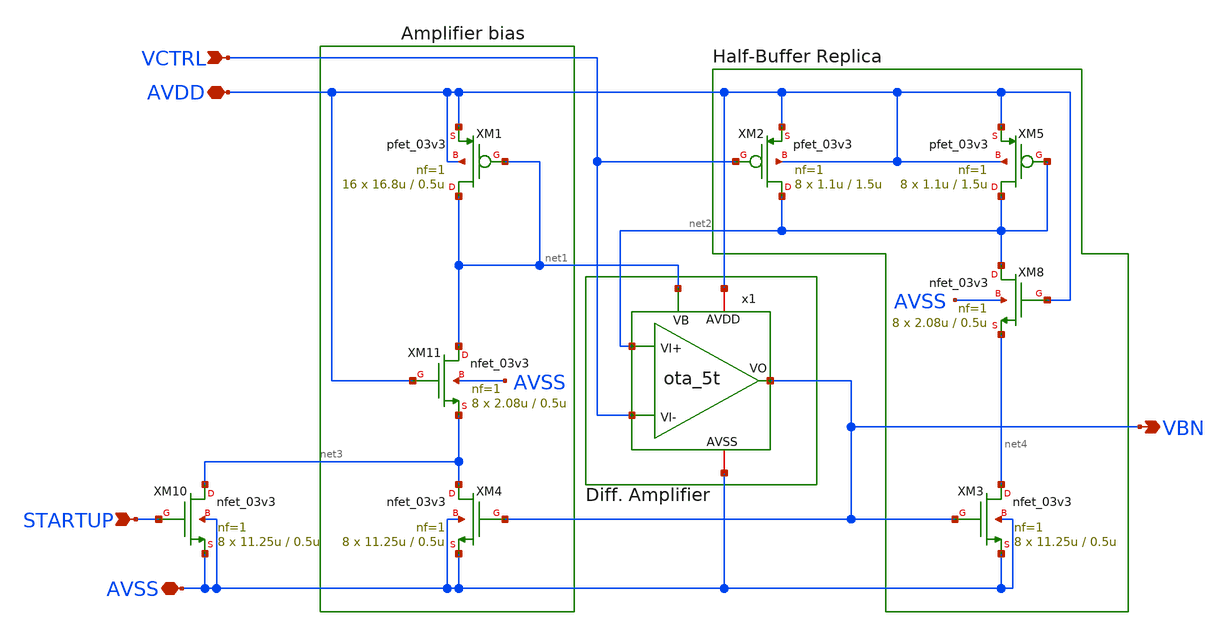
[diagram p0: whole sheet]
** sch_path: designs/libs/core_analog/bias_generator/bias_generator.sch
**.subckt bias_generator VCTRL STARTUP AVDD AVSS VBN
*.ipin VCTRL
*.ipin STARTUP
*.iopin AVDD
*.iopin AVSS
*.opin VBN
x1 VBN AVDD net2 VCTRL AVSS net1 ota_5t
XM1 net1 net1 AVDD AVDD pfet_03v3 L=0.5u W=16.8u nf=1 ad='int((nf+1)/2) * W/nf * 0.18u' as='int((nf+2)/2) * W/nf * 0.18u'
+ pd='2*int((nf+1)/2) * (W/nf + 0.18u)' ps='2*int((nf+2)/2) * (W/nf + 0.18u)' nrd='0.18u / W' nrs='0.18u / W'
+ sa=0 sb=0 sd=0 m=16
XM8 net2 AVDD net4 AVSS nfet_03v3 L=0.5u W=2.08u nf=1 ad='int((nf+1)/2) * W/nf * 0.18u' as='int((nf+2)/2) * W/nf * 0.18u'
+ pd='2*int((nf+1)/2) * (W/nf + 0.18u)' ps='2*int((nf+2)/2) * (W/nf + 0.18u)' nrd='0.18u / W' nrs='0.18u / W'
+ sa=0 sb=0 sd=0 m=8
XM11 net1 AVDD net3 AVSS nfet_03v3 L=0.5u W=2.08u nf=1 ad='int((nf+1)/2) * W/nf * 0.18u' as='int((nf+2)/2) * W/nf * 0.18u'
+ pd='2*int((nf+1)/2) * (W/nf + 0.18u)' ps='2*int((nf+2)/2) * (W/nf + 0.18u)' nrd='0.18u / W' nrs='0.18u / W'
+ sa=0 sb=0 sd=0 m=8
XM3 net4 VBN AVSS AVSS nfet_03v3 L=0.5u W=11.25u nf=1 ad='int((nf+1)/2) * W/nf * 0.18u' as='int((nf+2)/2) * W/nf * 0.18u'
+ pd='2*int((nf+1)/2) * (W/nf + 0.18u)' ps='2*int((nf+2)/2) * (W/nf + 0.18u)' nrd='0.18u / W' nrs='0.18u / W'
+ sa=0 sb=0 sd=0 m=8
XM4 net3 VBN AVSS AVSS nfet_03v3 L=0.5u W=11.25u nf=1 ad='int((nf+1)/2) * W/nf * 0.18u' as='int((nf+2)/2) * W/nf * 0.18u'
+ pd='2*int((nf+1)/2) * (W/nf + 0.18u)' ps='2*int((nf+2)/2) * (W/nf + 0.18u)' nrd='0.18u / W' nrs='0.18u / W'
+ sa=0 sb=0 sd=0 m=8
XM10 net3 STARTUP AVSS AVSS nfet_03v3 L=0.5u W=11.25u nf=1 ad='int((nf+1)/2) * W/nf * 0.18u' as='int((nf+2)/2) * W/nf * 0.18u'
+ pd='2*int((nf+1)/2) * (W/nf + 0.18u)' ps='2*int((nf+2)/2) * (W/nf + 0.18u)' nrd='0.18u / W' nrs='0.18u / W'
+ sa=0 sb=0 sd=0 m=8
XM2 net2 VCTRL AVDD AVDD pfet_03v3 L=1.5u W=1.1u nf=1 ad='int((nf+1)/2) * W/nf * 0.18u' as='int((nf+2)/2) * W/nf * 0.18u'
+ pd='2*int((nf+1)/2) * (W/nf + 0.18u)' ps='2*int((nf+2)/2) * (W/nf + 0.18u)' nrd='0.18u / W' nrs='0.18u / W'
+ sa=0 sb=0 sd=0 m=8
XM5 net2 net2 AVDD AVDD pfet_03v3 L=1.5u W=1.1u nf=1 ad='int((nf+1)/2) * W/nf * 0.18u' as='int((nf+2)/2) * W/nf * 0.18u'
+ pd='2*int((nf+1)/2) * (W/nf + 0.18u)' ps='2*int((nf+2)/2) * (W/nf + 0.18u)' nrd='0.18u / W' nrs='0.18u / W'
+ sa=0 sb=0 sd=0 m=8
**.ends

* expanding   symbol:  libs/core_analog/ota_5t/ota_5t.sym # of pins=6
** sym_path: designs/libs/core_analog/ota_5t/ota_5t.sym
** sch_path: designs/libs/core_analog/ota_5t/ota_5t.sch
.subckt ota_5t VO AVDD VI+ VI- AVSS VB
*.ipin VI+
*.ipin VI-
*.ipin VB
*.iopin AVDD
*.iopin AVSS
*.opin VO
XM1 VO VI- net2 AVDD pfet_03v3 L=0.5u W=6.55u nf=1 ad='int((nf+1)/2) * W/nf * 0.18u' as='int((nf+2)/2) * W/nf * 0.18u'
+ pd='2*int((nf+1)/2) * (W/nf + 0.18u)' ps='2*int((nf+2)/2) * (W/nf + 0.18u)' nrd='0.18u / W' nrs='0.18u / W'
+ sa=0 sb=0 sd=0 m=8
XM4 VO net1 AVSS AVSS nfet_03v3 L=0.5u W=4.8u nf=1 ad='int((nf+1)/2) * W/nf * 0.18u' as='int((nf+2)/2) * W/nf * 0.18u'
+ pd='2*int((nf+1)/2) * (W/nf + 0.18u)' ps='2*int((nf+2)/2) * (W/nf + 0.18u)' nrd='0.18u / W' nrs='0.18u / W'
+ sa=0 sb=0 sd=0 m=4
XM3 net2 VB net3 AVDD pfet_03v3 L=0.5u W=8.3u nf=1 ad='int((nf+1)/2) * W/nf * 0.18u' as='int((nf+2)/2) * W/nf * 0.18u'
+ pd='2*int((nf+1)/2) * (W/nf + 0.18u)' ps='2*int((nf+2)/2) * (W/nf + 0.18u)' nrd='0.18u / W' nrs='0.18u / W'
+ sa=0 sb=0 sd=0 m=16
XM2 net1 VI+ net2 AVDD pfet_03v3 L=0.5u W=6.55u nf=1 ad='int((nf+1)/2) * W/nf * 0.18u' as='int((nf+2)/2) * W/nf * 0.18u'
+ pd='2*int((nf+1)/2) * (W/nf + 0.18u)' ps='2*int((nf+2)/2) * (W/nf + 0.18u)' nrd='0.18u / W' nrs='0.18u / W'
+ sa=0 sb=0 sd=0 m=8
XM5 net1 net1 AVSS AVSS nfet_03v3 L=0.5u W=4.8u nf=1 ad='int((nf+1)/2) * W/nf * 0.18u' as='int((nf+2)/2) * W/nf * 0.18u'
+ pd='2*int((nf+1)/2) * (W/nf + 0.18u)' ps='2*int((nf+2)/2) * (W/nf + 0.18u)' nrd='0.18u / W' nrs='0.18u / W'
+ sa=0 sb=0 sd=0 m=4
Vmeas AVDD net3 0
.save i(vmeas)
.ends

.end
